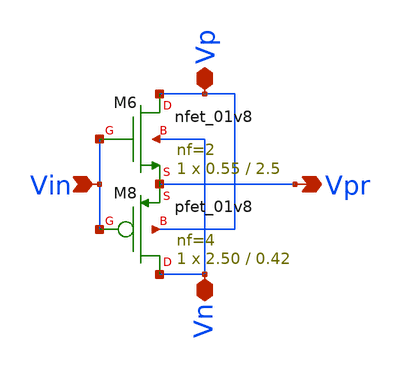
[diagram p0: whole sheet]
** sch_path: xschem/tr1/symbol/preamp_L.sch
**.subckt preamp_L Vin Vpr Vp Vn
*.ipin Vin
*.opin Vpr
*.iopin Vp
*.iopin Vn
XM6 Vp Vin Vpr Vn sky130_fd_pr__nfet_01v8 L=2.5 W=0.55 nf=2 ad='int((nf+1)/2) * W/nf * 0.29' as='int((nf+2)/2) * W/nf * 0.29'
+ pd='2*int((nf+1)/2) * (W/nf + 0.29)' ps='2*int((nf+2)/2) * (W/nf + 0.29)' nrd='0.29 / W' nrs='0.29 / W'
+ sa=0 sb=0 sd=0 mult=1 m=1
XM8 Vn Vin Vpr Vp sky130_fd_pr__pfet_01v8 L=0.42 W=2.50 nf=4 ad='int((nf+1)/2) * W/nf * 0.29' as='int((nf+2)/2) * W/nf * 0.29'
+ pd='2*int((nf+1)/2) * (W/nf + 0.29)' ps='2*int((nf+2)/2) * (W/nf + 0.29)' nrd='0.29 / W' nrs='0.29 / W'
+ sa=0 sb=0 sd=0 mult=1 m=1
**.ends
.end
